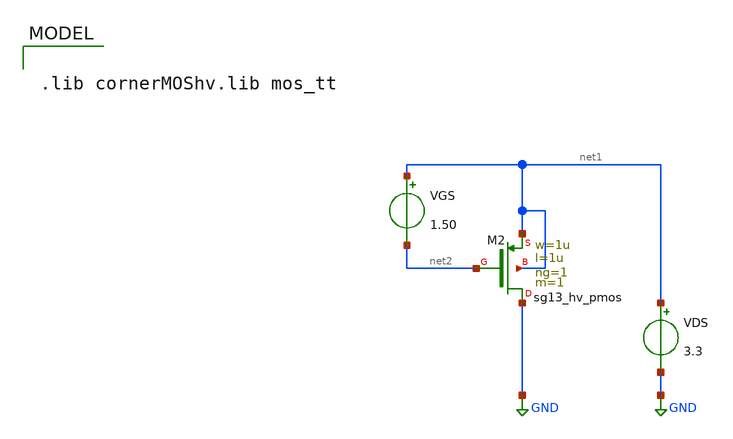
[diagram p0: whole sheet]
** sch_path: gmid/hv_pmos.sch
**.subckt hv_pmos
XM2 GND net2 net1 net1 sg13_hv_pmos w=1u l=1u ng=1 m=1 mm_ok=1
VGS net1 net2 1.50
VDS net1 GND 3.3
**** begin user architecture code

.lib cornerMOShv.lib mos_tt



.option savecurrents
.save all @n.xm2.nsg13_hv_pmos[ids] @n.xm2.nsg13_hv_pmos[l] @n.xm2.nsg13_hv_pmos[gm] @n.xm2.nsg13_hv_pmos[cgg] @n.xm2.nsg13_hv_pmos[gds] @n.xm2.nsg13_hv_pmos[vgs] @n.xm2.nsg13_hv_pmos[vds]
.control

.param L=1e-6

set wr_singlescale
set wr_vecnames
set appendwrite

let start_L = 1e-6
let stop_L = 50e-6
let delta_L = 1e-6

let start_VDS = 0
let stop_VDS = 3.4
let delta_VDS = 0.1

let actual_L = start_L

while actual_L le stop_L
	alter @n.xm2.nsg13_hv_pmos[l] = actual_L
	let actual_VDS = start_VDS
	while actual_VDS le stop_VDS
		alter VDS actual_VDS
		dc VGS 0 3.3 0.01
		wrdata hv_pmos.txt @n.xm2.nsg13_hv_pmos[vgs] @n.xm2.nsg13_hv_pmos[vds] @n.xm2.nsg13_hv_pmos[ids]
+ @n.xm2.nsg13_hv_pmos[l] @n.xm2.nsg13_hv_pmos[gm] @n.xm2.nsg13_hv_pmos[cgg] @n.xm2.nsg13_hv_pmos[gds]
		let actual_VDS = actual_VDS + delta_VDS
	end
	let actual_L = actual_L + delta_L
end

write hv_nmos.raw

.endc



**** end user architecture code
**.ends
.GLOBAL GND
.end
